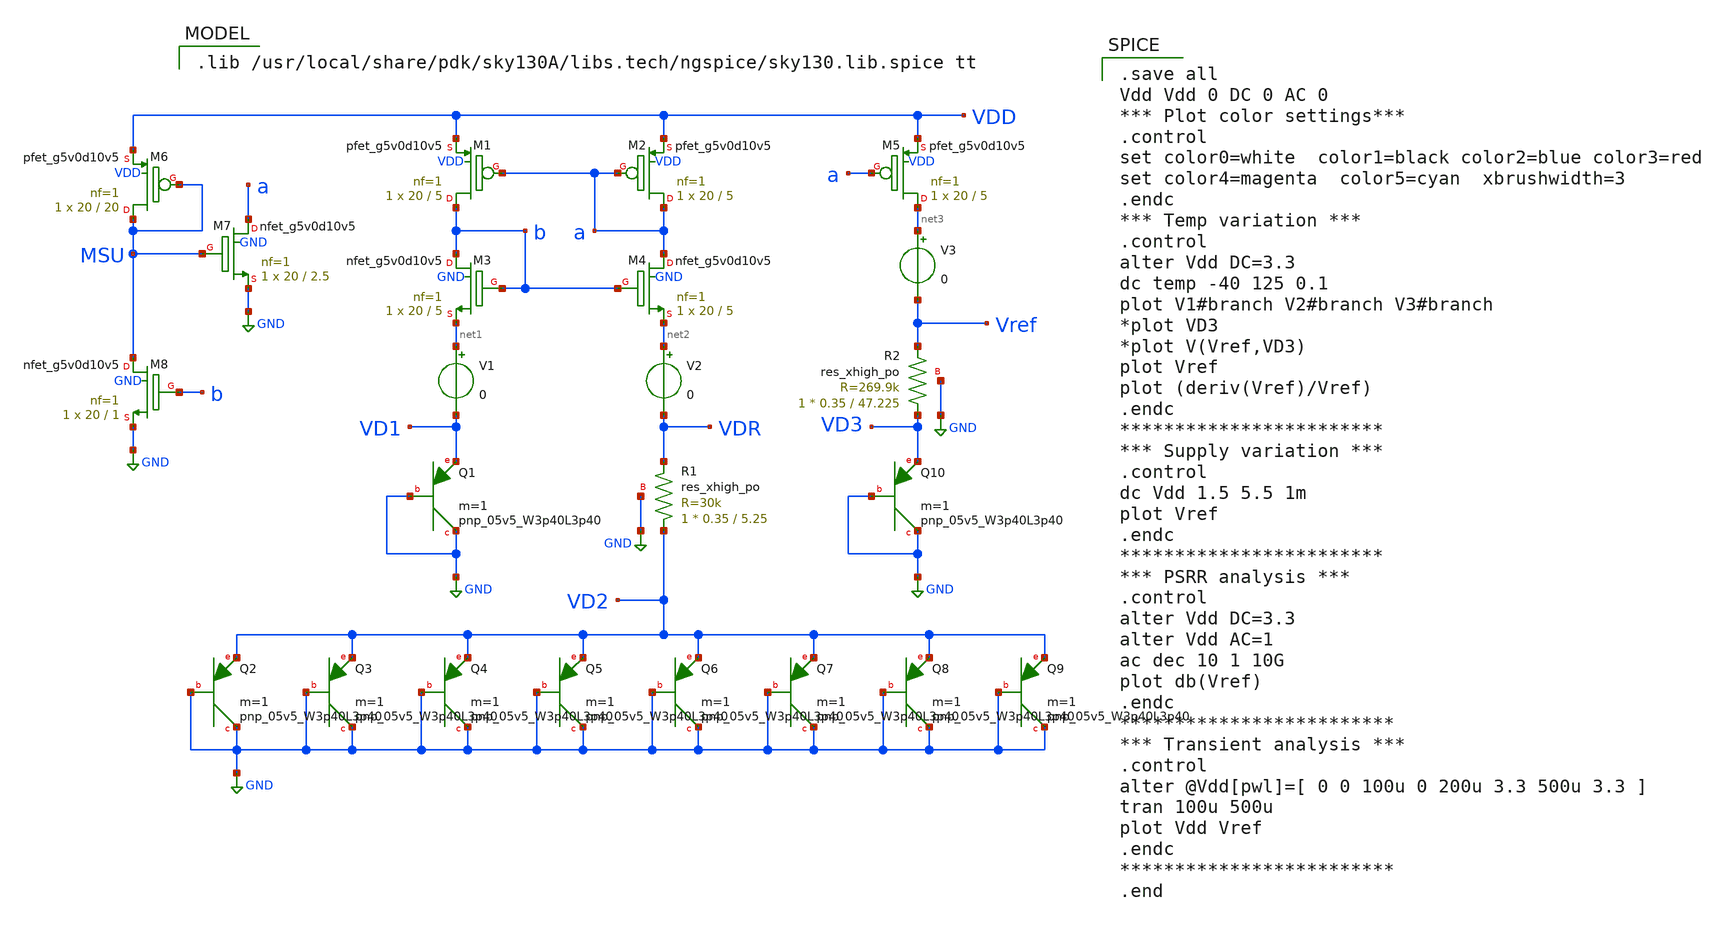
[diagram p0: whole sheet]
** sch_path: 2_BGR_nocas_30k_3p4pnp.sch
**.subckt 2_BGR_nocas_30k_3p4pnp
V1 net1 VD1 0
V2 net2 VDR 0
V3 net3 Vref 0
XM1 b a VDD VDD sky130_fd_pr__pfet_g5v0d10v5 L=5 W=20 nf=1 ad='int((nf+1)/2) * W/nf * 0.29' as='int((nf+2)/2) * W/nf * 0.29'
+ pd='2*int((nf+1)/2) * (W/nf + 0.29)' ps='2*int((nf+2)/2) * (W/nf + 0.29)' nrd='0.29 / W' nrs='0.29 / W'
+ sa=0 sb=0 sd=0 mult=1 m=1
XM2 a a VDD VDD sky130_fd_pr__pfet_g5v0d10v5 L=5 W=20 nf=1 ad='int((nf+1)/2) * W/nf * 0.29' as='int((nf+2)/2) * W/nf * 0.29'
+ pd='2*int((nf+1)/2) * (W/nf + 0.29)' ps='2*int((nf+2)/2) * (W/nf + 0.29)' nrd='0.29 / W' nrs='0.29 / W'
+ sa=0 sb=0 sd=0 mult=1 m=1
XM3 b b net1 GND sky130_fd_pr__nfet_g5v0d10v5 L=5 W=20 nf=1 ad='int((nf+1)/2) * W/nf * 0.29' as='int((nf+2)/2) * W/nf * 0.29'
+ pd='2*int((nf+1)/2) * (W/nf + 0.29)' ps='2*int((nf+2)/2) * (W/nf + 0.29)' nrd='0.29 / W' nrs='0.29 / W'
+ sa=0 sb=0 sd=0 mult=1 m=1
XM4 a b net2 GND sky130_fd_pr__nfet_g5v0d10v5 L=5 W=20 nf=1 ad='int((nf+1)/2) * W/nf * 0.29' as='int((nf+2)/2) * W/nf * 0.29'
+ pd='2*int((nf+1)/2) * (W/nf + 0.29)' ps='2*int((nf+2)/2) * (W/nf + 0.29)' nrd='0.29 / W' nrs='0.29 / W'
+ sa=0 sb=0 sd=0 mult=1 m=1
XM5 net3 a VDD VDD sky130_fd_pr__pfet_g5v0d10v5 L=5 W=20 nf=1 ad='int((nf+1)/2) * W/nf * 0.29' as='int((nf+2)/2) * W/nf * 0.29'
+ pd='2*int((nf+1)/2) * (W/nf + 0.29)' ps='2*int((nf+2)/2) * (W/nf + 0.29)' nrd='0.29 / W' nrs='0.29 / W'
+ sa=0 sb=0 sd=0 mult=1 m=1
XM8 MSU b GND GND sky130_fd_pr__nfet_g5v0d10v5 L=1 W=20 nf=1 ad='int((nf+1)/2) * W/nf * 0.29' as='int((nf+2)/2) * W/nf * 0.29'
+ pd='2*int((nf+1)/2) * (W/nf + 0.29)' ps='2*int((nf+2)/2) * (W/nf + 0.29)' nrd='0.29 / W' nrs='0.29 / W'
+ sa=0 sb=0 sd=0 mult=1 m=1
XM7 a MSU GND GND sky130_fd_pr__nfet_g5v0d10v5 L=2.5 W=20 nf=1 ad='int((nf+1)/2) * W/nf * 0.29' as='int((nf+2)/2) * W/nf * 0.29'
+ pd='2*int((nf+1)/2) * (W/nf + 0.29)' ps='2*int((nf+2)/2) * (W/nf + 0.29)' nrd='0.29 / W' nrs='0.29 / W'
+ sa=0 sb=0 sd=0 mult=1 m=1
XQ1 GND GND VD1 sky130_fd_pr__pnp_05v5_W3p40L3p40 m=1
XQ2 GND GND VD2 sky130_fd_pr__pnp_05v5_W3p40L3p40 m=1
XQ3 GND GND VD2 sky130_fd_pr__pnp_05v5_W3p40L3p40 m=1
XQ4 GND GND VD2 sky130_fd_pr__pnp_05v5_W3p40L3p40 m=1
XQ5 GND GND VD2 sky130_fd_pr__pnp_05v5_W3p40L3p40 m=1
XQ6 GND GND VD2 sky130_fd_pr__pnp_05v5_W3p40L3p40 m=1
XQ7 GND GND VD2 sky130_fd_pr__pnp_05v5_W3p40L3p40 m=1
XQ8 GND GND VD2 sky130_fd_pr__pnp_05v5_W3p40L3p40 m=1
XQ9 GND GND VD2 sky130_fd_pr__pnp_05v5_W3p40L3p40 m=1
XQ10 GND GND VD3 sky130_fd_pr__pnp_05v5_W3p40L3p40 m=1
XM6 MSU MSU VDD VDD sky130_fd_pr__pfet_g5v0d10v5 L=20 W=20 nf=1 ad='int((nf+1)/2) * W/nf * 0.29' as='int((nf+2)/2) * W/nf * 0.29'
+ pd='2*int((nf+1)/2) * (W/nf + 0.29)' ps='2*int((nf+2)/2) * (W/nf + 0.29)' nrd='0.29 / W' nrs='0.29 / W'
+ sa=0 sb=0 sd=0 mult=1 m=1
XR1 VD2 VDR GND sky130_fd_pr__res_xhigh_po W=0.35 L=5.25 mult=1 m=1
XR2 VD3 Vref GND sky130_fd_pr__res_xhigh_po W=0.35 L=47.225 mult=1 m=1
**** begin user architecture code

.lib /usr/local/share/pdk/sky130A/libs.tech/ngspice/sky130.lib.spice tt


.save all
Vdd Vdd 0 DC 0 AC 0
*** Plot color settings***
.control
set color0=white  color1=black color2=blue color3=red
set color4=magenta  color5=cyan  xbrushwidth=3
.endc
*** Temp variation ***
.control
alter Vdd DC=3.3
dc temp -40 125 0.1
plot V1#branch V2#branch V3#branch
*plot VD3
*plot V(Vref,VD3)
plot Vref
plot (deriv(Vref)/Vref)
.endc
************************
*** Supply variation ***
.control
dc Vdd 1.5 5.5 1m
plot Vref
.endc
************************
*** PSRR analysis ***
.control
alter Vdd DC=3.3
alter Vdd AC=1
ac dec 10 1 10G
plot db(Vref)
.endc
*************************
*** Transient analysis ***
.control
alter @Vdd[pwl]=[ 0 0 100u 0 200u 3.3 500u 3.3 ]
tran 100u 500u
plot Vdd Vref
.endc
*************************
.end

**** end user architecture code
**.ends
.GLOBAL GND
.end
